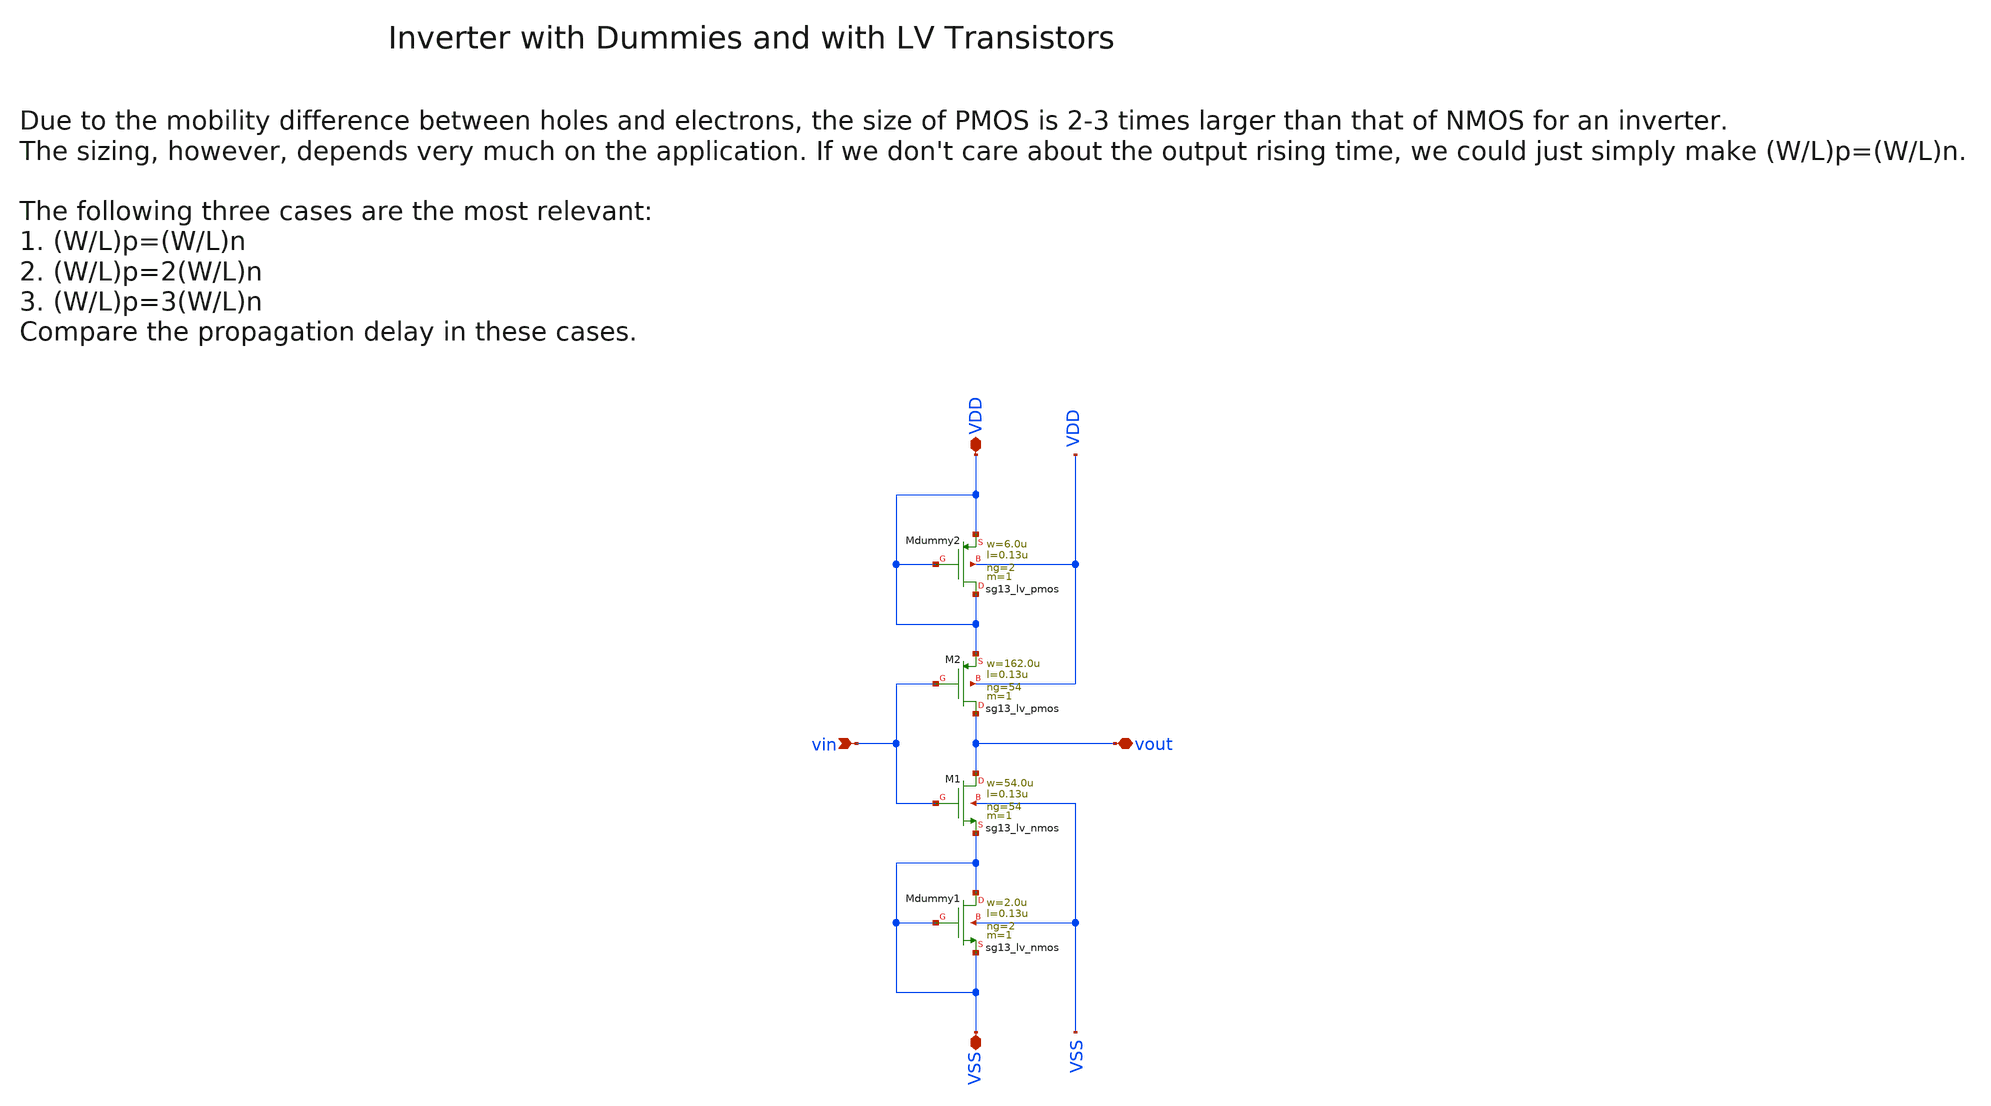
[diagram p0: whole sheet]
** sch_path: ihp130/macros/iqmod/schematic/xschem/iqmod_mixer_se2diff_inv_NF54.sch
**.subckt iqmod_mixer_se2diff_inv_NF54 vin VDD VSS vout
*.ipin vin
*.iopin VDD
*.iopin VSS
*.iopin vout
XM1 vout vin VSS VSS sg13_lv_nmos w=54.0u l=0.13u ng=54 m=1 mm_ok=1
XM2 vout vin VDD VDD sg13_lv_pmos w=162.0u l=0.13u ng=54 m=1 mm_ok=1
XMdummy1 VSS VSS VSS VSS sg13_lv_nmos w=2.0u l=0.13u ng=2 m=1 mm_ok=1
XMdummy2 VDD VDD VDD VDD sg13_lv_pmos w=6.0u l=0.13u ng=2 m=1 mm_ok=1
**.ends
.end
